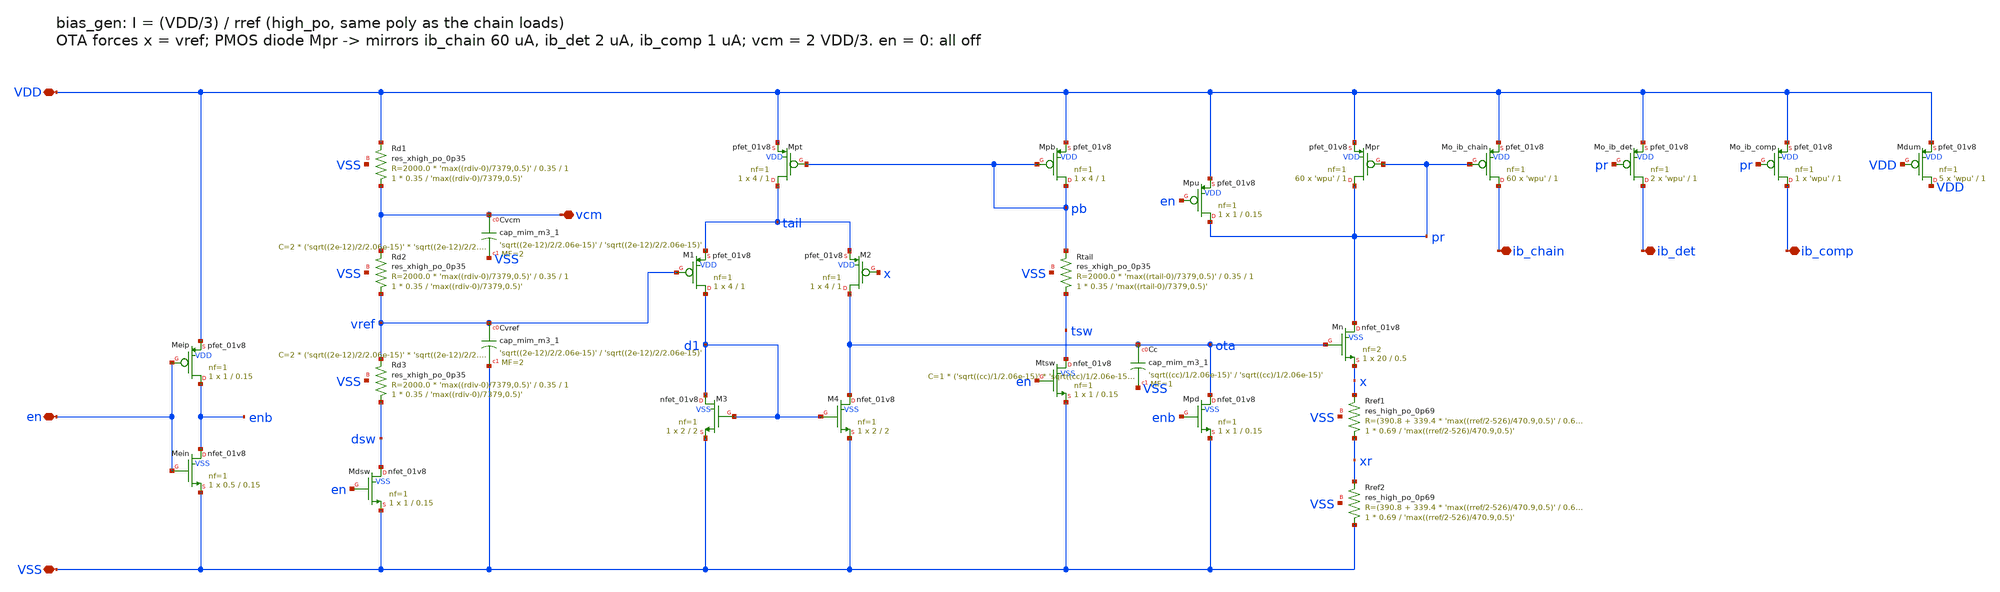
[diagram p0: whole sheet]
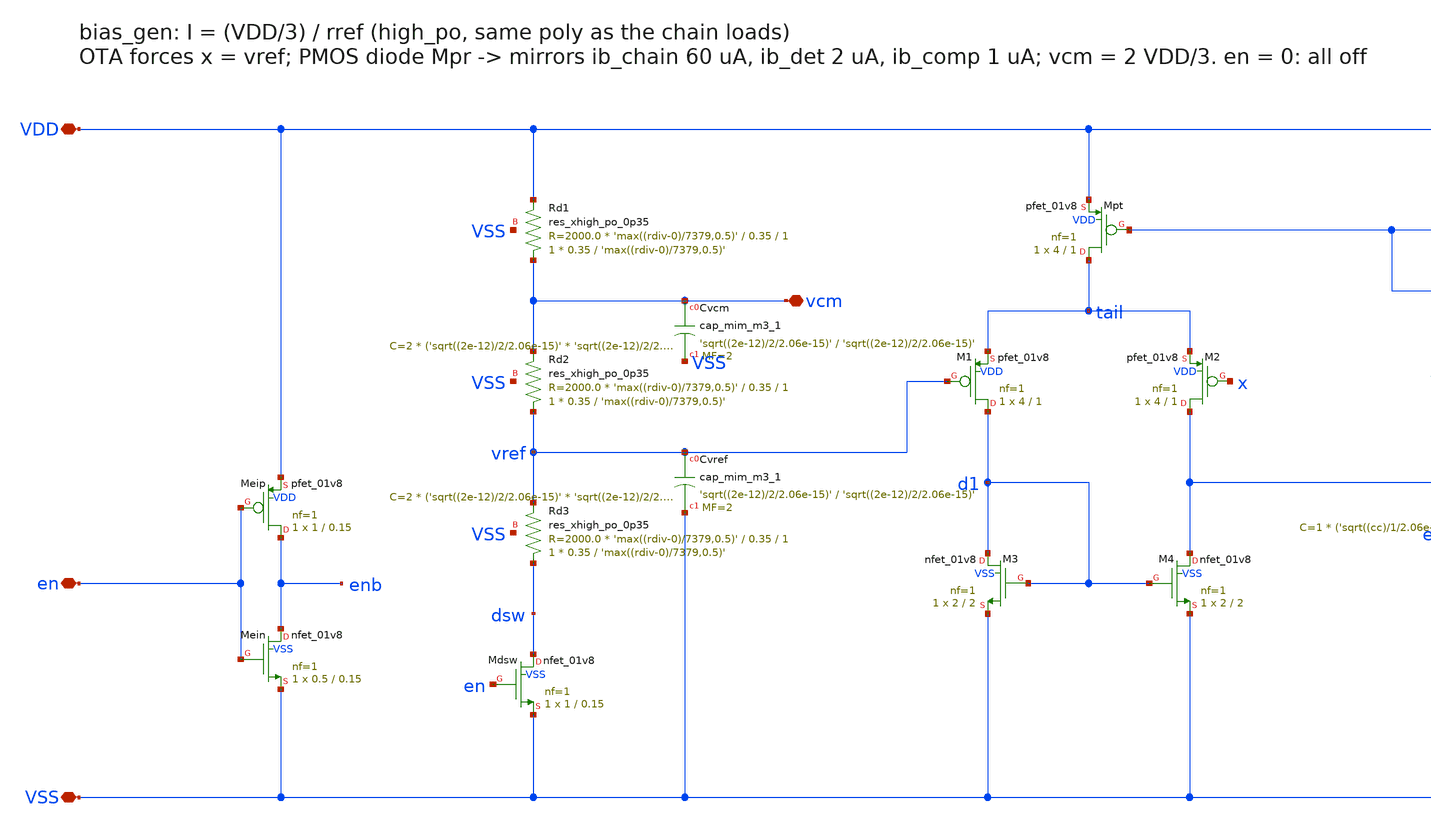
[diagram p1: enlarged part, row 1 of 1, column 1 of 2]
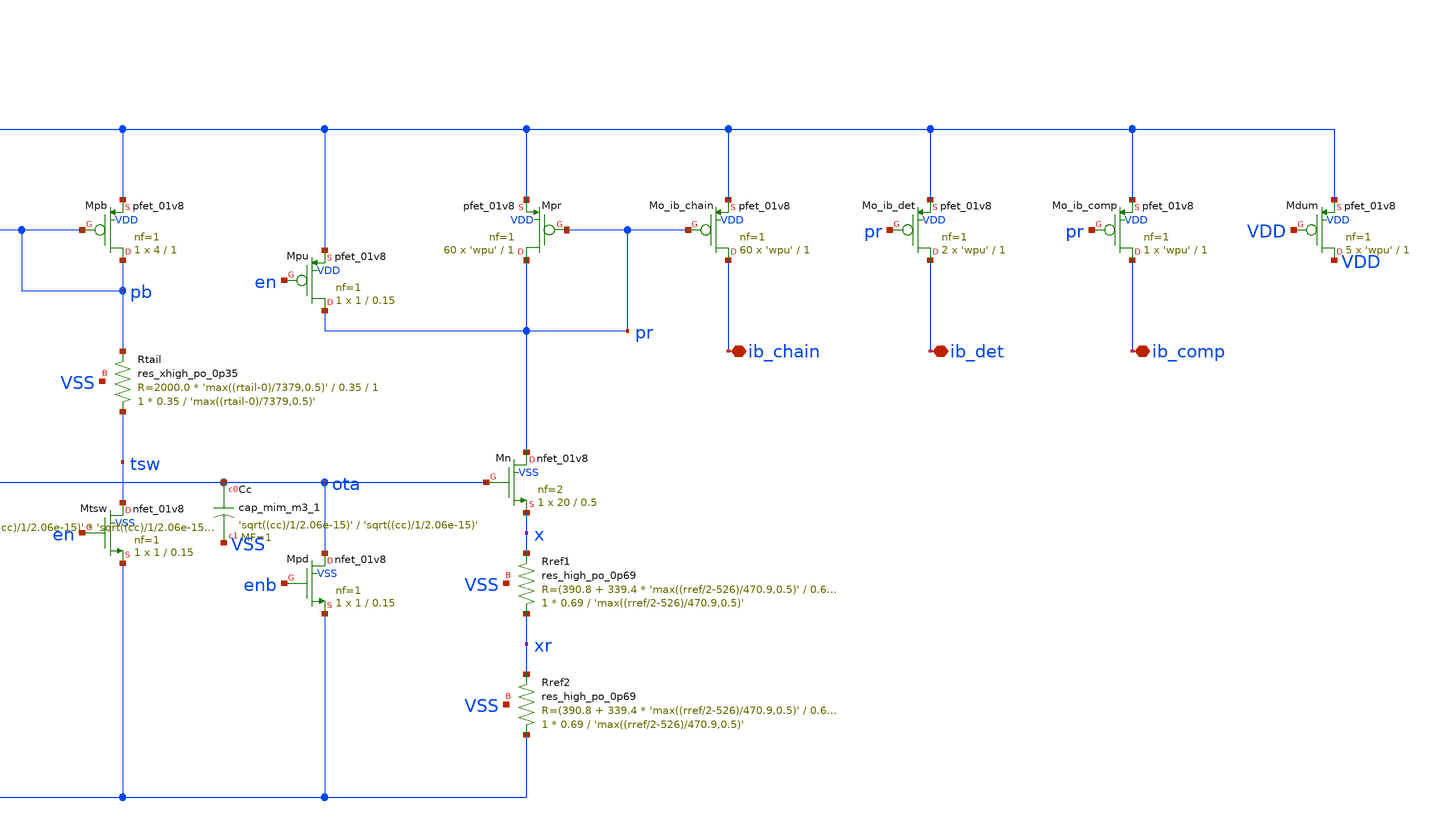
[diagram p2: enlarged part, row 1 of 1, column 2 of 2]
** sch_path: xschem/bias_gen.sch
**.subckt bias_gen VDD VSS en vcm ib_chain ib_det ib_comp
*.iopin VDD
*.iopin VSS
*.iopin en
*.iopin vcm
*.iopin ib_chain
*.iopin ib_det
*.iopin ib_comp
XMeip enb en VDD VDD sky130_fd_pr__pfet_01v8 L=0.15 W=1 nf=1 ad='int((nf+1)/2) * W/nf * 0.29' as='int((nf+2)/2) * W/nf * 0.29'
+ pd='2*int((nf+1)/2) * (W/nf + 0.29)' ps='2*int((nf+2)/2) * (W/nf + 0.29)' nrd='0.29 / W' nrs='0.29 / W'
+ sa=0 sb=0 sd=0 mult=1 m=1
XMein enb en VSS VSS sky130_fd_pr__nfet_01v8 L=0.15 W=0.5 nf=1 ad='int((nf+1)/2) * W/nf * 0.29' as='int((nf+2)/2) * W/nf * 0.29'
+ pd='2*int((nf+1)/2) * (W/nf + 0.29)' ps='2*int((nf+2)/2) * (W/nf + 0.29)' nrd='0.29 / W' nrs='0.29 / W'
+ sa=0 sb=0 sd=0 mult=1 m=1
XRd1 vcm VDD VSS sky130_fd_pr__res_xhigh_po_0p35 L='max((rdiv-0)/7379,0.5)' mult=1 m=1
XRd2 vref vcm VSS sky130_fd_pr__res_xhigh_po_0p35 L='max((rdiv-0)/7379,0.5)' mult=1 m=1
XRd3 dsw vref VSS sky130_fd_pr__res_xhigh_po_0p35 L='max((rdiv-0)/7379,0.5)' mult=1 m=1
XMdsw dsw en VSS VSS sky130_fd_pr__nfet_01v8 L=0.15 W=1 nf=1 ad='int((nf+1)/2) * W/nf * 0.29' as='int((nf+2)/2) * W/nf * 0.29'
+ pd='2*int((nf+1)/2) * (W/nf + 0.29)' ps='2*int((nf+2)/2) * (W/nf + 0.29)' nrd='0.29 / W' nrs='0.29 / W'
+ sa=0 sb=0 sd=0 mult=1 m=1
XCvcm vcm VSS sky130_fd_pr__cap_mim_m3_1 W='sqrt((2e-12)/2/2.06e-15)' L='sqrt((2e-12)/2/2.06e-15)' MF=2
+ m=2
XCvref vref VSS sky130_fd_pr__cap_mim_m3_1 W='sqrt((2e-12)/2/2.06e-15)' L='sqrt((2e-12)/2/2.06e-15)'
+ MF=2 m=2
XMpb pb pb VDD VDD sky130_fd_pr__pfet_01v8 L=1 W=4 nf=1 ad='int((nf+1)/2) * W/nf * 0.29' as='int((nf+2)/2) * W/nf * 0.29'
+ pd='2*int((nf+1)/2) * (W/nf + 0.29)' ps='2*int((nf+2)/2) * (W/nf + 0.29)' nrd='0.29 / W' nrs='0.29 / W'
+ sa=0 sb=0 sd=0 mult=1 m=1
XRtail tsw pb VSS sky130_fd_pr__res_xhigh_po_0p35 L='max((rtail-0)/7379,0.5)' mult=1 m=1
XMtsw tsw en VSS VSS sky130_fd_pr__nfet_01v8 L=0.15 W=1 nf=1 ad='int((nf+1)/2) * W/nf * 0.29' as='int((nf+2)/2) * W/nf * 0.29'
+ pd='2*int((nf+1)/2) * (W/nf + 0.29)' ps='2*int((nf+2)/2) * (W/nf + 0.29)' nrd='0.29 / W' nrs='0.29 / W'
+ sa=0 sb=0 sd=0 mult=1 m=1
XMpt tail pb VDD VDD sky130_fd_pr__pfet_01v8 L=1 W=4 nf=1 ad='int((nf+1)/2) * W/nf * 0.29' as='int((nf+2)/2) * W/nf * 0.29'
+ pd='2*int((nf+1)/2) * (W/nf + 0.29)' ps='2*int((nf+2)/2) * (W/nf + 0.29)' nrd='0.29 / W' nrs='0.29 / W'
+ sa=0 sb=0 sd=0 mult=1 m=1
XM1 d1 vref tail VDD sky130_fd_pr__pfet_01v8 L=1 W=4 nf=1 ad='int((nf+1)/2) * W/nf * 0.29' as='int((nf+2)/2) * W/nf * 0.29'
+ pd='2*int((nf+1)/2) * (W/nf + 0.29)' ps='2*int((nf+2)/2) * (W/nf + 0.29)' nrd='0.29 / W' nrs='0.29 / W'
+ sa=0 sb=0 sd=0 mult=1 m=1
XM2 ota x tail VDD sky130_fd_pr__pfet_01v8 L=1 W=4 nf=1 ad='int((nf+1)/2) * W/nf * 0.29' as='int((nf+2)/2) * W/nf * 0.29'
+ pd='2*int((nf+1)/2) * (W/nf + 0.29)' ps='2*int((nf+2)/2) * (W/nf + 0.29)' nrd='0.29 / W' nrs='0.29 / W'
+ sa=0 sb=0 sd=0 mult=1 m=1
XM3 d1 d1 VSS VSS sky130_fd_pr__nfet_01v8 L=2 W=2 nf=1 ad='int((nf+1)/2) * W/nf * 0.29' as='int((nf+2)/2) * W/nf * 0.29'
+ pd='2*int((nf+1)/2) * (W/nf + 0.29)' ps='2*int((nf+2)/2) * (W/nf + 0.29)' nrd='0.29 / W' nrs='0.29 / W'
+ sa=0 sb=0 sd=0 mult=1 m=1
XM4 ota d1 VSS VSS sky130_fd_pr__nfet_01v8 L=2 W=2 nf=1 ad='int((nf+1)/2) * W/nf * 0.29' as='int((nf+2)/2) * W/nf * 0.29'
+ pd='2*int((nf+1)/2) * (W/nf + 0.29)' ps='2*int((nf+2)/2) * (W/nf + 0.29)' nrd='0.29 / W' nrs='0.29 / W'
+ sa=0 sb=0 sd=0 mult=1 m=1
XCc ota VSS sky130_fd_pr__cap_mim_m3_1 W='sqrt((cc)/1/2.06e-15)' L='sqrt((cc)/1/2.06e-15)' MF=1 m=1
XMpd ota enb VSS VSS sky130_fd_pr__nfet_01v8 L=0.15 W=1 nf=1 ad='int((nf+1)/2) * W/nf * 0.29' as='int((nf+2)/2) * W/nf * 0.29'
+ pd='2*int((nf+1)/2) * (W/nf + 0.29)' ps='2*int((nf+2)/2) * (W/nf + 0.29)' nrd='0.29 / W' nrs='0.29 / W'
+ sa=0 sb=0 sd=0 mult=1 m=1
XMn pr ota x VSS sky130_fd_pr__nfet_01v8 L=0.5 W=20 nf=2 ad='int((nf+1)/2) * W/nf * 0.29' as='int((nf+2)/2) * W/nf * 0.29'
+ pd='2*int((nf+1)/2) * (W/nf + 0.29)' ps='2*int((nf+2)/2) * (W/nf + 0.29)' nrd='0.29 / W' nrs='0.29 / W'
+ sa=0 sb=0 sd=0 mult=1 m=1
XRref1 xr x VSS sky130_fd_pr__res_high_po_0p69 L='max((rref/2-526)/470.9,0.5)' mult=1 m=1
XRref2 VSS xr VSS sky130_fd_pr__res_high_po_0p69 L='max((rref/2-526)/470.9,0.5)' mult=1 m=1
XMpr pr pr VDD VDD sky130_fd_pr__pfet_01v8 L=1 W='wpu' nf=1 ad='int((nf+1)/2) * W/nf * 0.29' as='int((nf+2)/2) * W/nf * 0.29'
+ pd='2*int((nf+1)/2) * (W/nf + 0.29)' ps='2*int((nf+2)/2) * (W/nf + 0.29)' nrd='0.29 / W' nrs='0.29 / W'
+ sa=0 sb=0 sd=0 mult=60 m=60
XMpu pr en VDD VDD sky130_fd_pr__pfet_01v8 L=0.15 W=1 nf=1 ad='int((nf+1)/2) * W/nf * 0.29' as='int((nf+2)/2) * W/nf * 0.29'
+ pd='2*int((nf+1)/2) * (W/nf + 0.29)' ps='2*int((nf+2)/2) * (W/nf + 0.29)' nrd='0.29 / W' nrs='0.29 / W'
+ sa=0 sb=0 sd=0 mult=1 m=1
XMo_ib_chain ib_chain pr VDD VDD sky130_fd_pr__pfet_01v8 L=1 W='wpu' nf=1 ad='int((nf+1)/2) * W/nf * 0.29'
+ as='int((nf+2)/2) * W/nf * 0.29' pd='2*int((nf+1)/2) * (W/nf + 0.29)' ps='2*int((nf+2)/2) * (W/nf + 0.29)'
+ nrd='0.29 / W' nrs='0.29 / W' sa=0 sb=0 sd=0 mult=60 m=60
XMo_ib_det ib_det pr VDD VDD sky130_fd_pr__pfet_01v8 L=1 W='wpu' nf=1 ad='int((nf+1)/2) * W/nf * 0.29'
+ as='int((nf+2)/2) * W/nf * 0.29' pd='2*int((nf+1)/2) * (W/nf + 0.29)' ps='2*int((nf+2)/2) * (W/nf + 0.29)'
+ nrd='0.29 / W' nrs='0.29 / W' sa=0 sb=0 sd=0 mult=2 m=2
XMo_ib_comp ib_comp pr VDD VDD sky130_fd_pr__pfet_01v8 L=1 W='wpu' nf=1 ad='int((nf+1)/2) * W/nf * 0.29'
+ as='int((nf+2)/2) * W/nf * 0.29' pd='2*int((nf+1)/2) * (W/nf + 0.29)' ps='2*int((nf+2)/2) * (W/nf + 0.29)'
+ nrd='0.29 / W' nrs='0.29 / W' sa=0 sb=0 sd=0 mult=1 m=1
XMdum VDD VDD VDD VDD sky130_fd_pr__pfet_01v8 L=1 W='wpu' nf=1 ad='int((nf+1)/2) * W/nf * 0.29' as='int((nf+2)/2) * W/nf * 0.29'
+ pd='2*int((nf+1)/2) * (W/nf + 0.29)' ps='2*int((nf+2)/2) * (W/nf + 0.29)' nrd='0.29 / W' nrs='0.29 / W'
+ sa=0 sb=0 sd=0 mult=5 m=5
**.ends
.end
